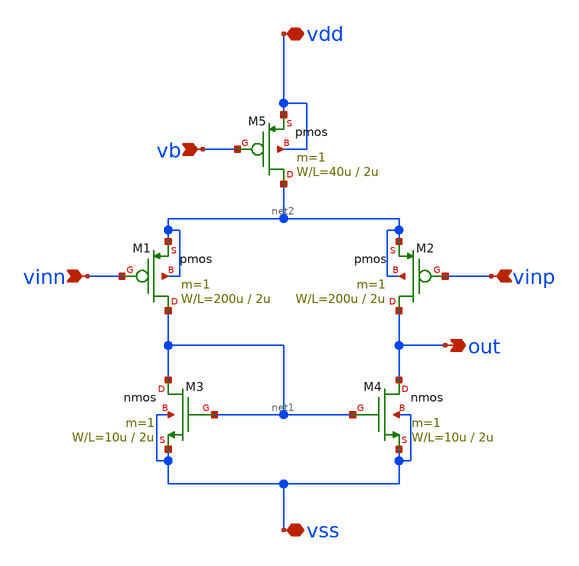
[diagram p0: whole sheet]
** sch_path: OR1/PTC06/opamp/diff.sch
**.subckt diff vinn vinp vb out vdd vss
*.ipin vinn
*.ipin vinp
*.ipin vb
*.opin out
*.iopin vdd
*.iopin vss
M5 net2 vb vdd vdd pmos L=2u W=40u m=1
M1 net1 vinn net2 net2 pmos L=2u W=200u m=1
M2 out vinp net2 net2 pmos L=2u W=200u m=1
M3 net1 net1 vss vss nmos L=2u W=10u m=1
M4 out net1 vss vss nmos L=2u W=10u m=1
**.ends
.end
